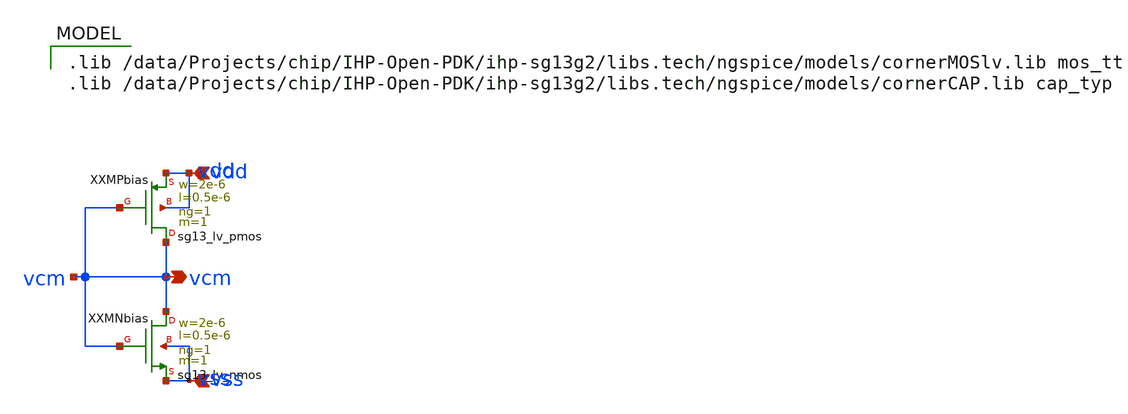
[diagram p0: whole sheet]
** sch_path: xschem/bias_gen.sch
**.subckt bias_gen vcm vdd vss
*.opin vcm
*.ipin vdd
*.ipin vss
XXXMPbias vcm vcm vdd vdd sg13_lv_pmos w=2e-6 l=0.5e-6 ng=1 m=1 mm_ok=1
XXXMNbias vcm vcm vss vss sg13_lv_nmos w=2e-6 l=0.5e-6 ng=1 m=1 mm_ok=1
**** begin user architecture code
 .lib /data/Projects/chip/IHP-Open-PDK/ihp-sg13g2/libs.tech/ngspice/models/cornerMOSlv.lib mos_tt
.lib /data/Projects/chip/IHP-Open-PDK/ihp-sg13g2/libs.tech/ngspice/models/cornerCAP.lib cap_typ

**** end user architecture code
**.ends
.end
